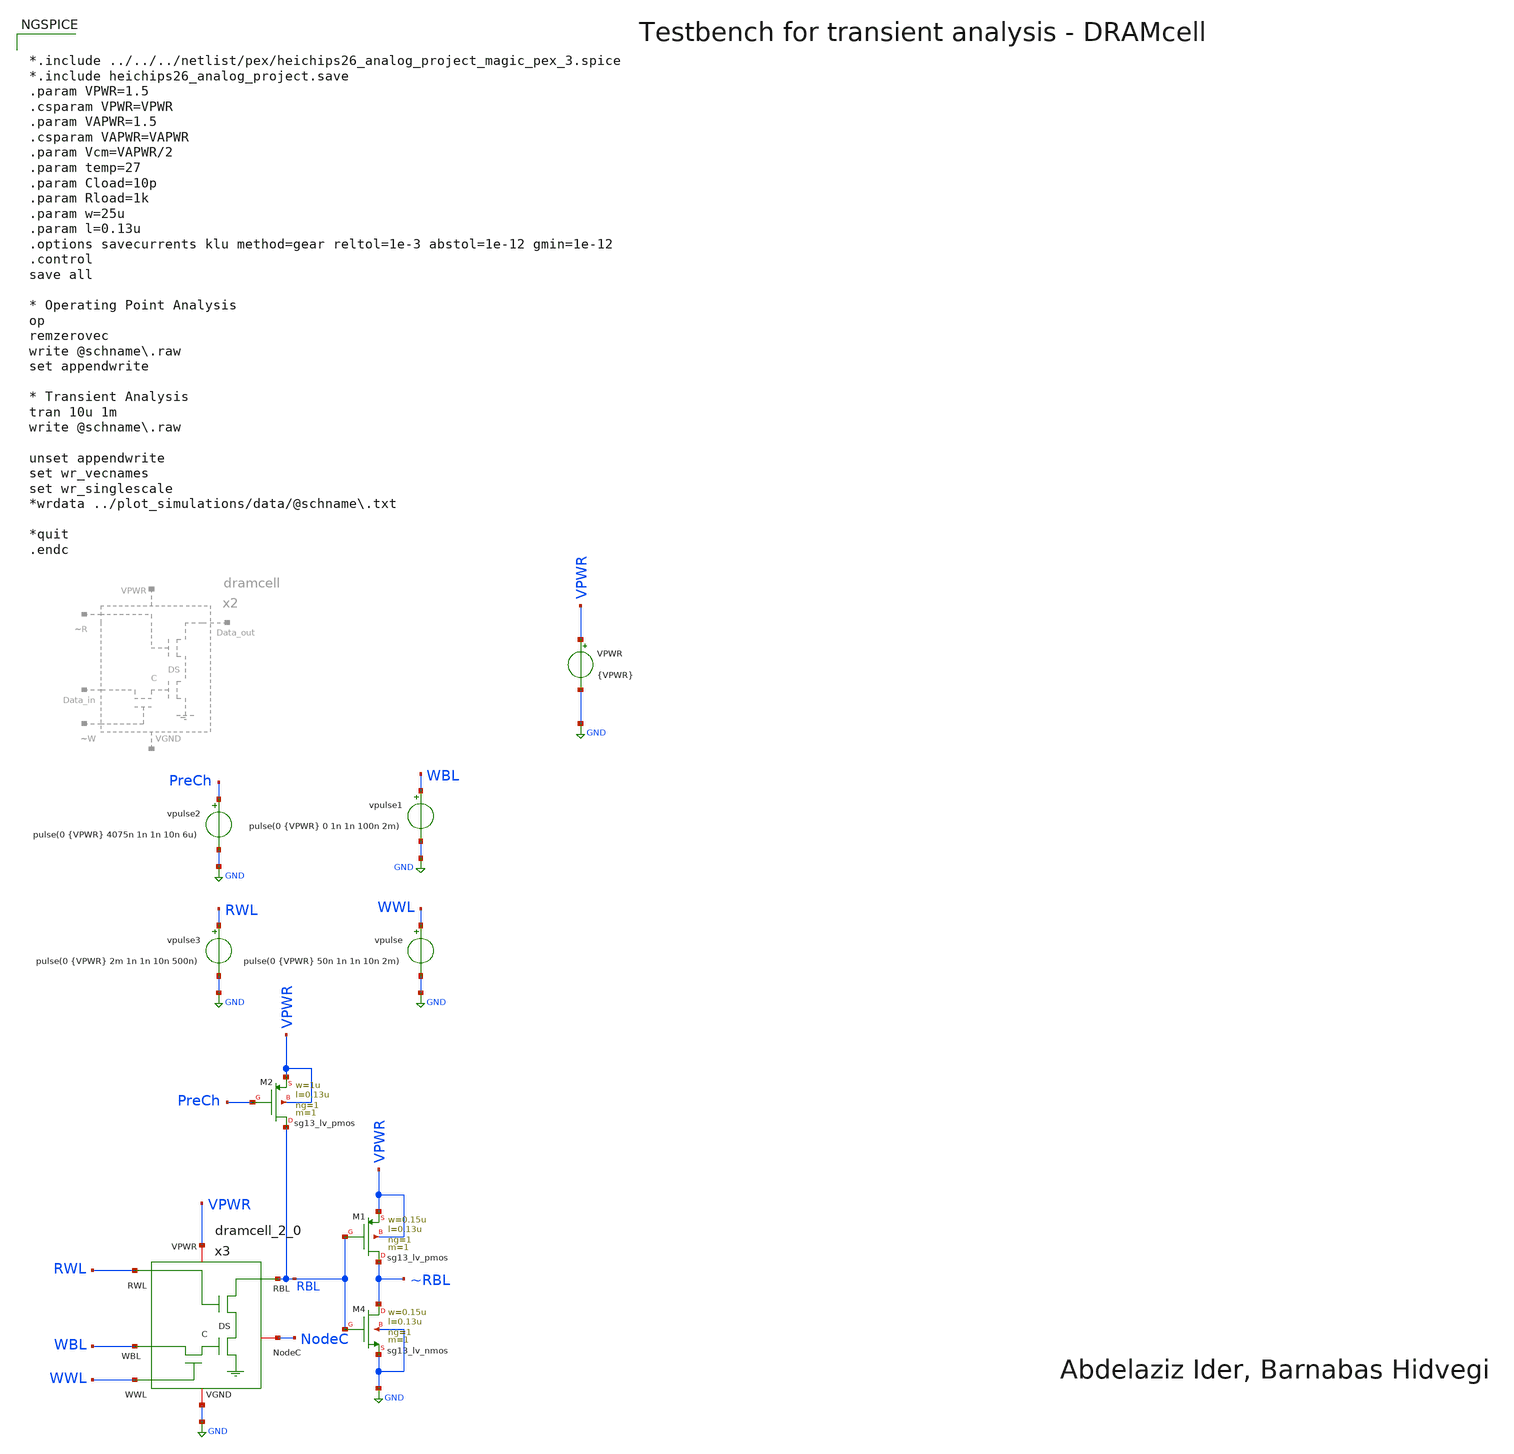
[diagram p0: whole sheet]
** sch_path: macros/heichips26_analog_project/macros/dramcell_2_0/testbenches/xschem/inverter_tb_tran.sch
**.subckt inverter_tb_tran
vpulse WWL GND pulse(0 {VPWR} 50n 1n 1n 10n 2m)
VPWR VPWR GND {VPWR}
XM2 RBL PreCh VPWR VPWR sg13_lv_pmos w=1u l=0.13u ng=1 m=1 mm_ok=1
vpulse1 WBL GND pulse(0 {VPWR} 0 1n 1n 100n 2m)
vpulse2 PreCh GND pulse(0 {VPWR} 4075n 1n 1n 10n 6u)
vpulse3 RWL GND pulse(0 {VPWR} 2m 1n 1n 10n 500n)
x3 WWL WBL RWL RBL GND VPWR NodeC dramcell_2_0
XM1 ~RBL RBL VPWR VPWR sg13_lv_pmos w=0.15u l=0.13u ng=1 m=1 mm_ok=1
XM4 ~RBL RBL GND GND sg13_lv_nmos w=0.15u l=0.13u ng=1 m=1 mm_ok=1
**** begin user architecture code


*.include ../../../netlist/pex/heichips26_analog_project_magic_pex_3.spice
*.include heichips26_analog_project.save
.param VPWR=1.5
.csparam VPWR=VPWR
.param VAPWR=1.5
.csparam VAPWR=VAPWR
.param Vcm=VAPWR/2
.param temp=27
.param Cload=10p
.param Rload=1k
.param w=25u
.param l=0.13u
.options savecurrents klu method=gear reltol=1e-3 abstol=1e-12 gmin=1e-12
.control
save all

* Operating Point Analysis
op
remzerovec
write @schname\.raw
set appendwrite

* Transient Analysis
tran 10u 1m
write @schname\.raw

unset appendwrite
set wr_vecnames
set wr_singlescale
*wrdata ../plot_simulations/data/@schname\.txt

*quit
.endc



.lib cornerMOSlv.lib mos_tt
.lib cornerMOShv.lib mos_tt
.lib cornerRES.lib res_typ
.lib cornerDIO.lib dio_tt
.lib cornerCAP.lib cap_typ

**** end user architecture code
**.ends
.GLOBAL GND
.end
